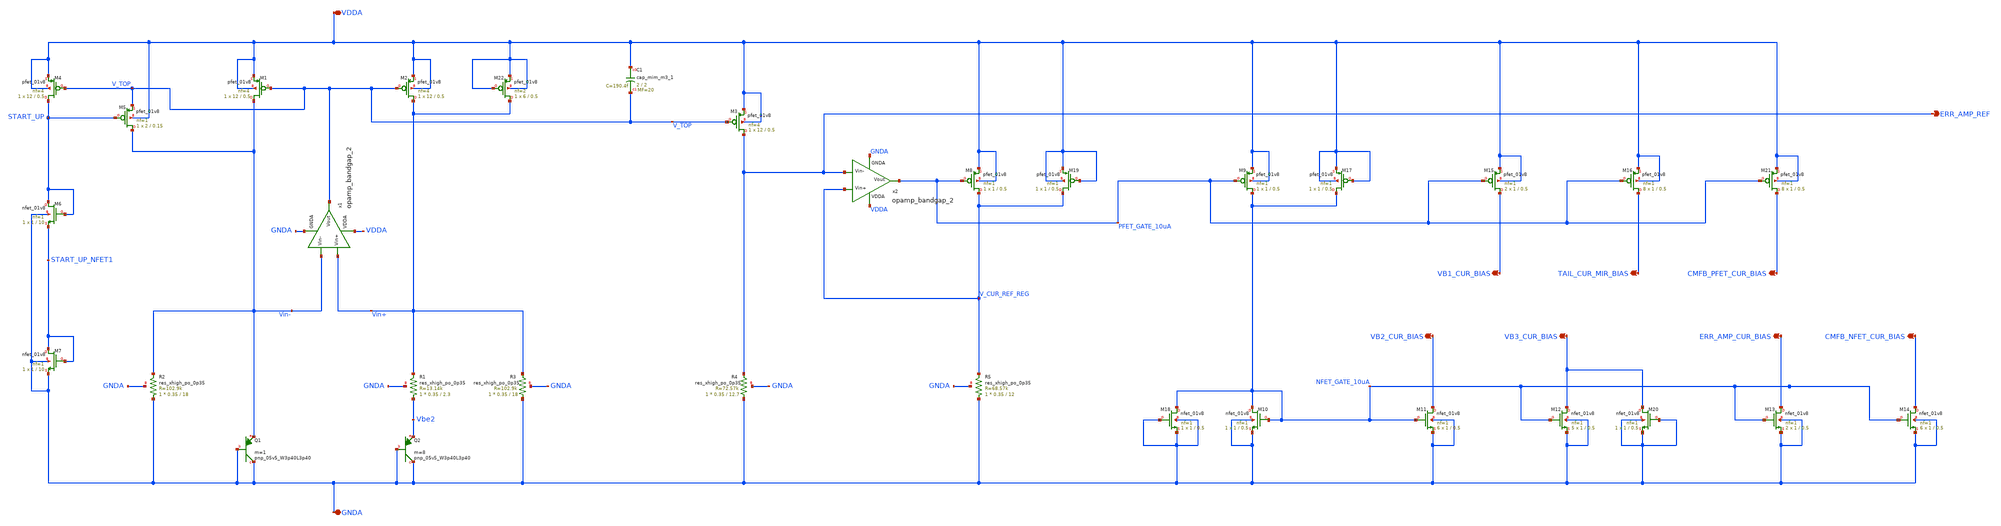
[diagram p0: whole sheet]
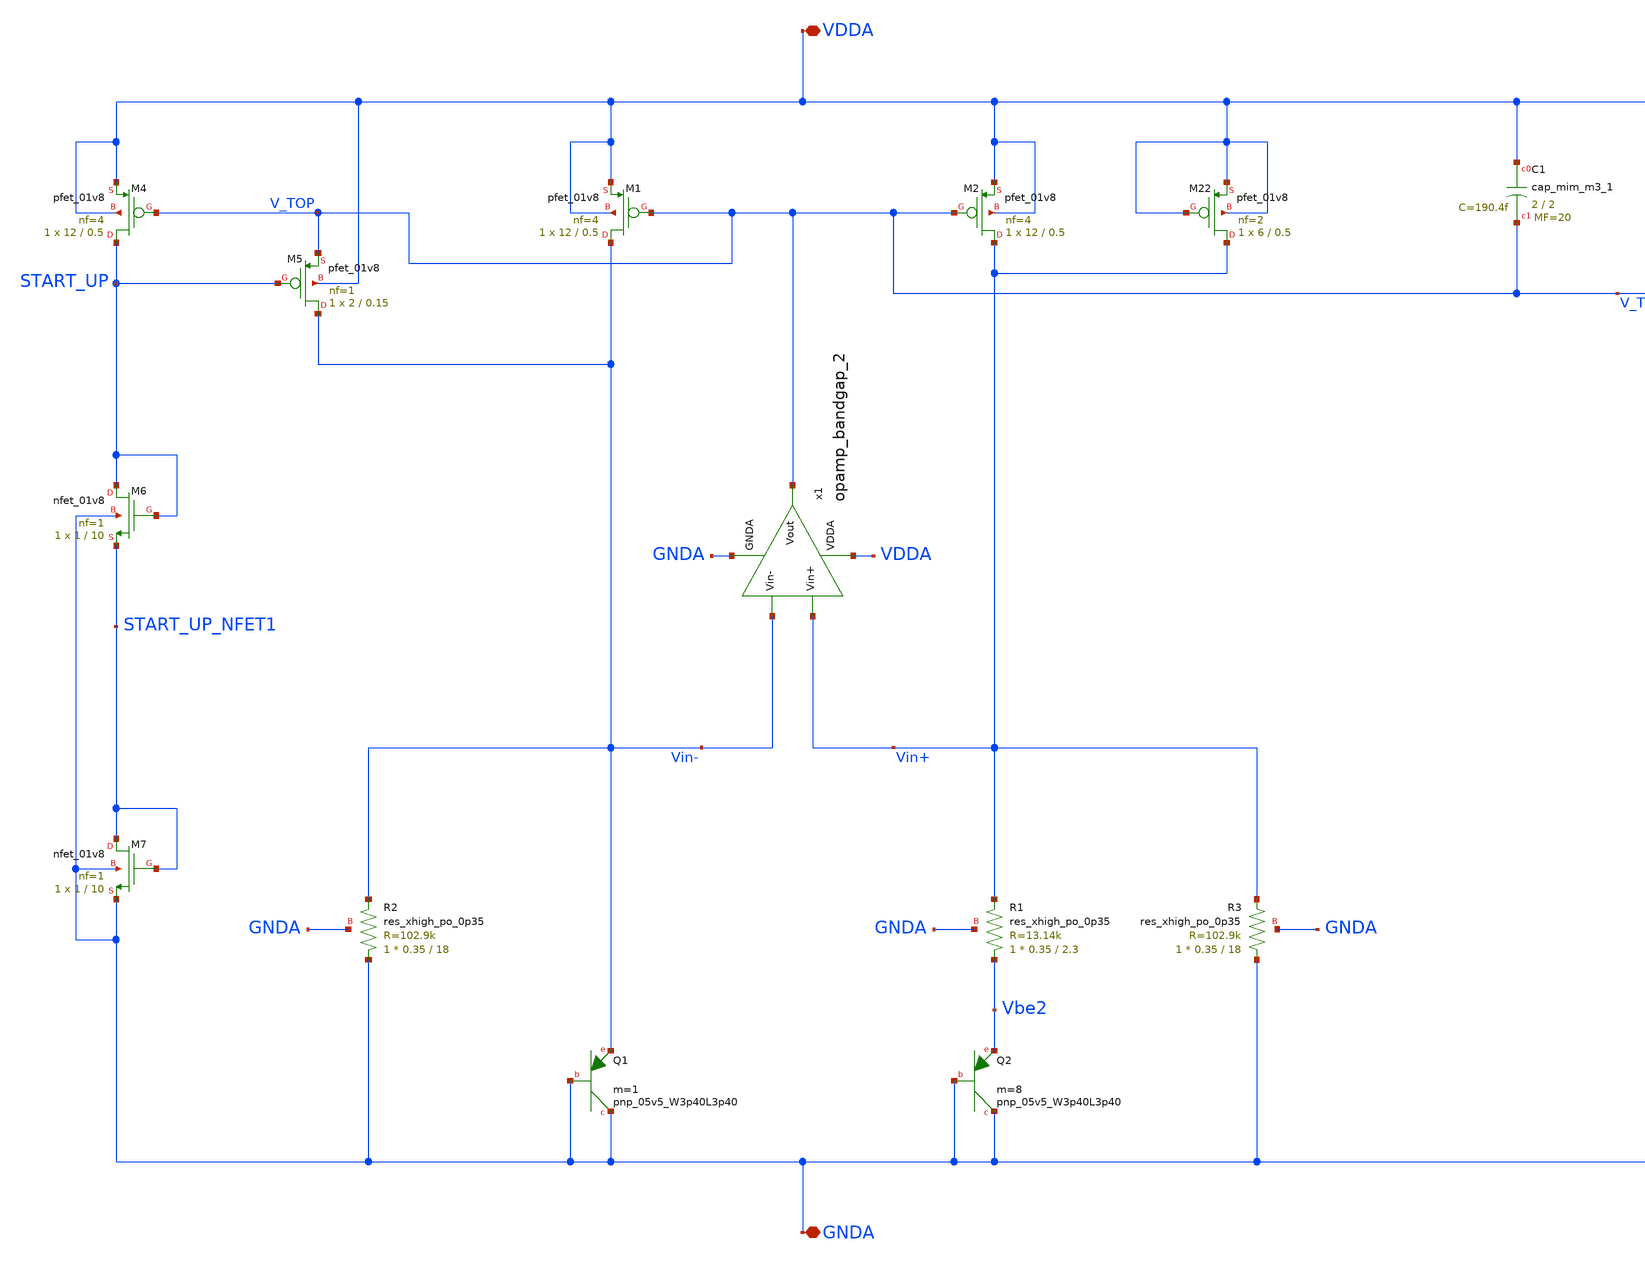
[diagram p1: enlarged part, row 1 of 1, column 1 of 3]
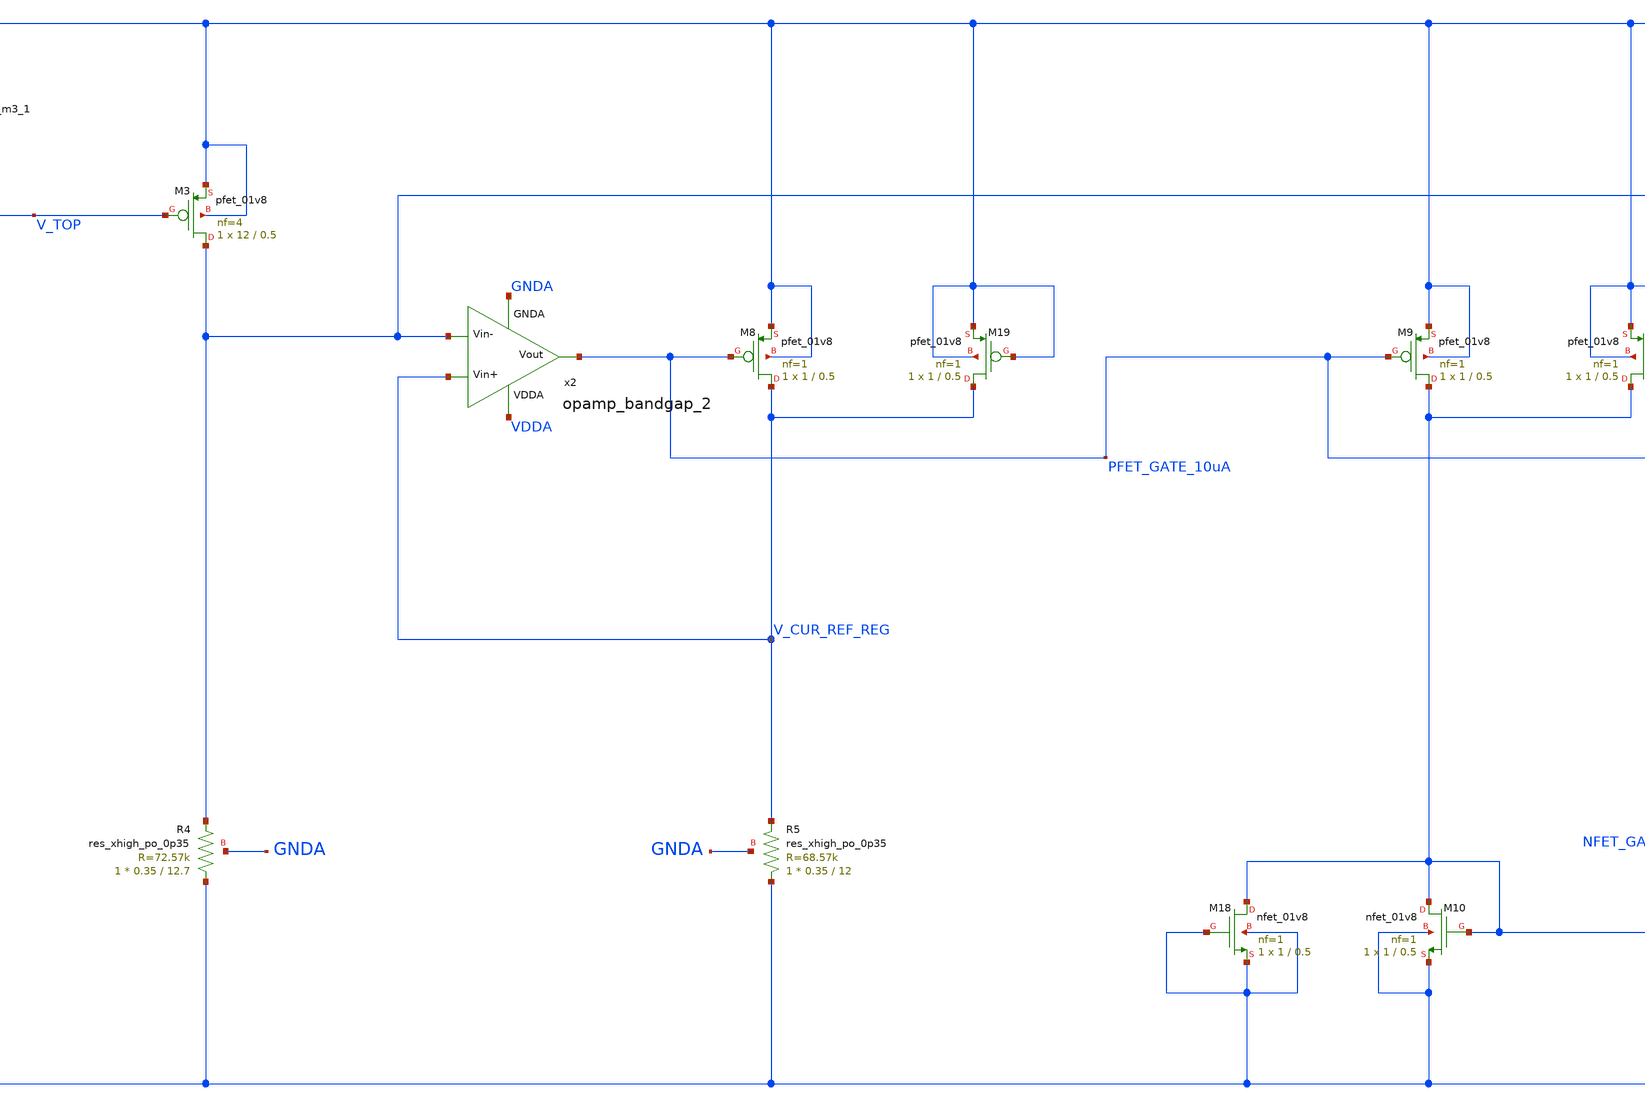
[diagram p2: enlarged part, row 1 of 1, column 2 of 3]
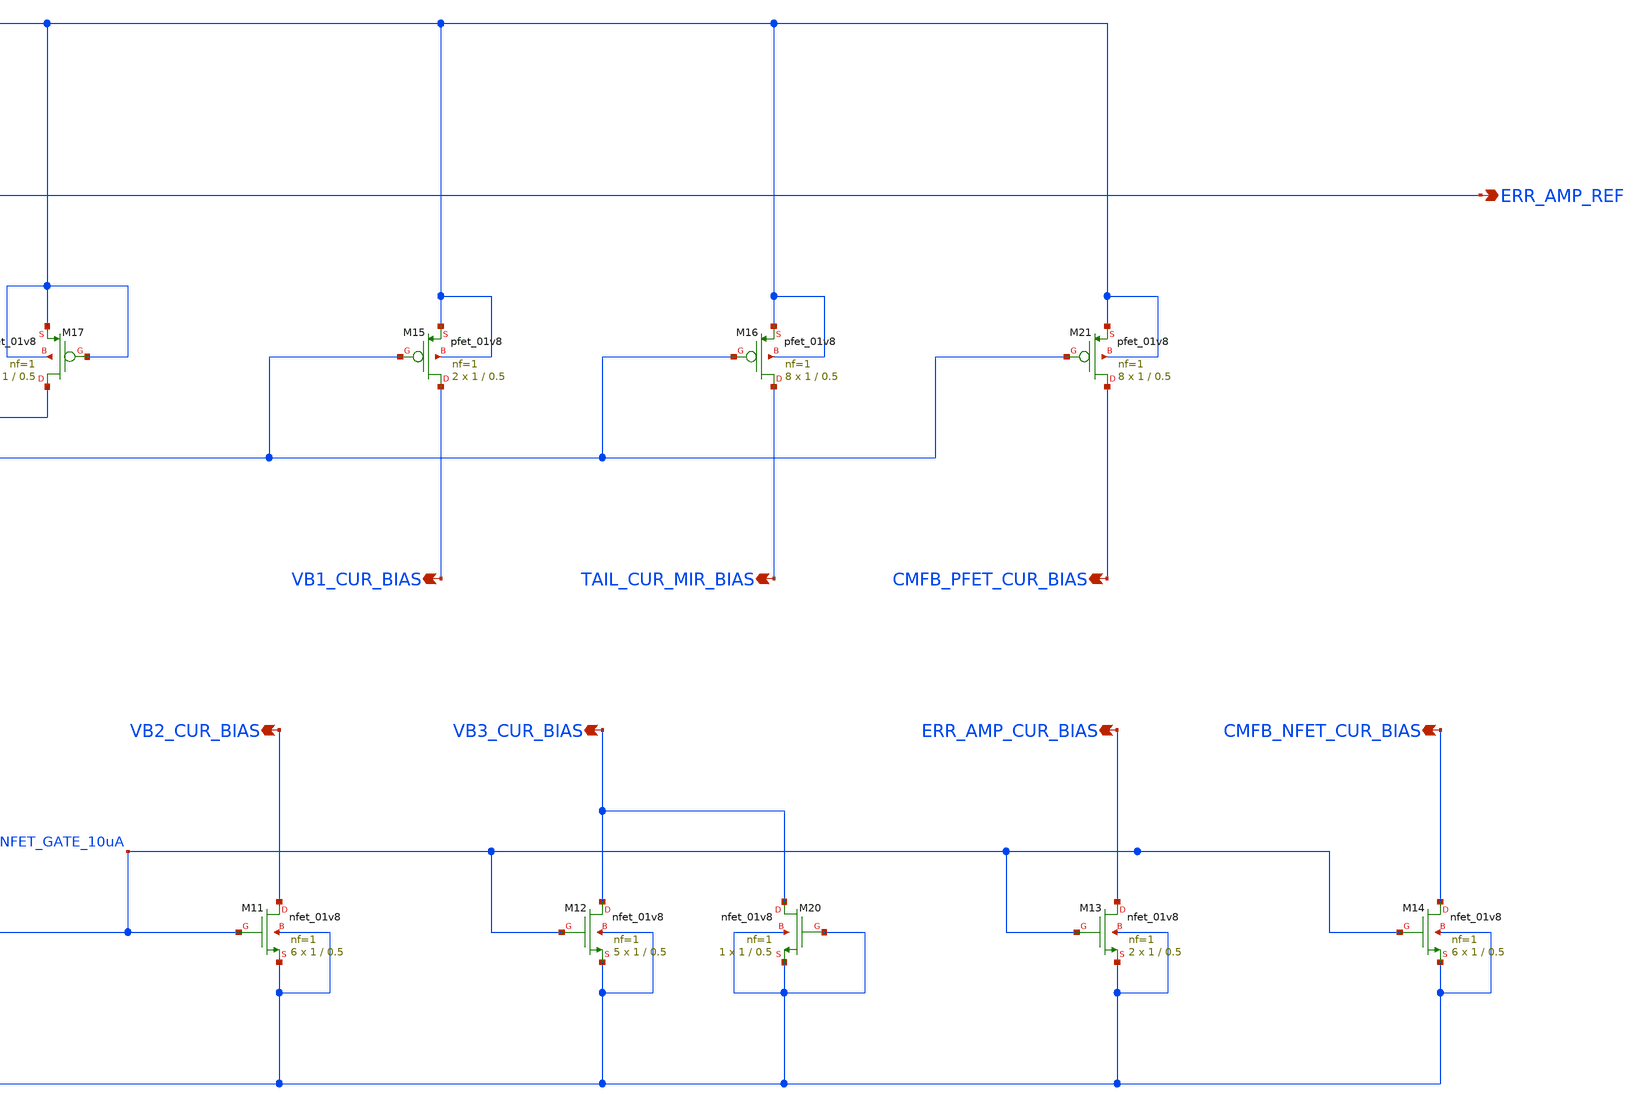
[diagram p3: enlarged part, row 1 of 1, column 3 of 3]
** sch_path: projects/opamp/xschem_ngspice/ref_volt_cur_gen_dummy.sch
**.subckt ref_volt_cur_gen_dummy VB1_CUR_BIAS GNDA ERR_AMP_REF VDDA VB2_CUR_BIAS VB3_CUR_BIAS
*+ ERR_AMP_CUR_BIAS CMFB_NFET_CUR_BIAS TAIL_CUR_MIR_BIAS CMFB_PFET_CUR_BIAS
*.opin VB1_CUR_BIAS
*.iopin GNDA
*.opin ERR_AMP_REF
*.iopin VDDA
*.opin VB2_CUR_BIAS
*.opin VB3_CUR_BIAS
*.opin ERR_AMP_CUR_BIAS
*.opin CMFB_NFET_CUR_BIAS
*.opin TAIL_CUR_MIR_BIAS
*.opin CMFB_PFET_CUR_BIAS
XM3 ERR_AMP_REF V_TOP VDDA VDDA sky130_fd_pr__pfet_01v8 L=0.5 W=12 nf=4 ad='int((nf+1)/2) * W/nf * 0.29'
+ as='int((nf+2)/2) * W/nf * 0.29' pd='2*int((nf+1)/2) * (W/nf + 0.29)' ps='2*int((nf+2)/2) * (W/nf + 0.29)'
+ nrd='0.29 / W' nrs='0.29 / W' sa=0 sb=0 sd=0 mult=1 m=1
XR4 GNDA ERR_AMP_REF GNDA sky130_fd_pr__res_xhigh_po_0p35 L=12.7 mult=1 m=1
XR5 GNDA V_CUR_REF_REG GNDA sky130_fd_pr__res_xhigh_po_0p35 L=12 mult=1 m=1
XM8 V_CUR_REF_REG PFET_GATE_10uA VDDA VDDA sky130_fd_pr__pfet_01v8 L=0.5 W=1 nf=1 ad='int((nf+1)/2) * W/nf * 0.29'
+ as='int((nf+2)/2) * W/nf * 0.29' pd='2*int((nf+1)/2) * (W/nf + 0.29)' ps='2*int((nf+2)/2) * (W/nf + 0.29)'
+ nrd='0.29 / W' nrs='0.29 / W' sa=0 sb=0 sd=0 mult=1 m=1
XC1 VDDA V_TOP sky130_fd_pr__cap_mim_m3_1 W=2 L=2 MF=20 m=20
XQ1 GNDA GNDA Vin- sky130_fd_pr__pnp_05v5_W3p40L3p40 m=1
XQ2 GNDA GNDA Vbe2 sky130_fd_pr__pnp_05v5_W3p40L3p40 m=8
XM1 Vin- V_TOP VDDA VDDA sky130_fd_pr__pfet_01v8 L=0.5 W=12 nf=4 ad='int((nf+1)/2) * W/nf * 0.29' as='int((nf+2)/2) * W/nf * 0.29'
+ pd='2*int((nf+1)/2) * (W/nf + 0.29)' ps='2*int((nf+2)/2) * (W/nf + 0.29)' nrd='0.29 / W' nrs='0.29 / W'
+ sa=0 sb=0 sd=0 mult=1 m=1
XM2 Vin+ V_TOP VDDA VDDA sky130_fd_pr__pfet_01v8 L=0.5 W=12 nf=4 ad='int((nf+1)/2) * W/nf * 0.29' as='int((nf+2)/2) * W/nf * 0.29'
+ pd='2*int((nf+1)/2) * (W/nf + 0.29)' ps='2*int((nf+2)/2) * (W/nf + 0.29)' nrd='0.29 / W' nrs='0.29 / W'
+ sa=0 sb=0 sd=0 mult=1 m=1
XR1 Vbe2 Vin+ GNDA sky130_fd_pr__res_xhigh_po_0p35 L=2.3 mult=1 m=1
XR3 GNDA Vin+ GNDA sky130_fd_pr__res_xhigh_po_0p35 L=18 mult=1 m=1
XR2 GNDA Vin- GNDA sky130_fd_pr__res_xhigh_po_0p35 L=18 mult=1 m=1
XM6 START_UP START_UP START_UP_NFET1 GNDA sky130_fd_pr__nfet_01v8 L=10 W=1 nf=1 ad='int((nf+1)/2) * W/nf * 0.29'
+ as='int((nf+2)/2) * W/nf * 0.29' pd='2*int((nf+1)/2) * (W/nf + 0.29)' ps='2*int((nf+2)/2) * (W/nf + 0.29)'
+ nrd='0.29 / W' nrs='0.29 / W' sa=0 sb=0 sd=0 mult=1 m=1
XM4 START_UP V_TOP VDDA VDDA sky130_fd_pr__pfet_01v8 L=0.5 W=12 nf=4 ad='int((nf+1)/2) * W/nf * 0.29'
+ as='int((nf+2)/2) * W/nf * 0.29' pd='2*int((nf+1)/2) * (W/nf + 0.29)' ps='2*int((nf+2)/2) * (W/nf + 0.29)'
+ nrd='0.29 / W' nrs='0.29 / W' sa=0 sb=0 sd=0 mult=1 m=1
XM5 Vin- START_UP V_TOP VDDA sky130_fd_pr__pfet_01v8 L=0.15 W=2 nf=1 ad='int((nf+1)/2) * W/nf * 0.29'
+ as='int((nf+2)/2) * W/nf * 0.29' pd='2*int((nf+1)/2) * (W/nf + 0.29)' ps='2*int((nf+2)/2) * (W/nf + 0.29)'
+ nrd='0.29 / W' nrs='0.29 / W' sa=0 sb=0 sd=0 mult=1 m=1
XM7 START_UP_NFET1 START_UP_NFET1 GNDA GNDA sky130_fd_pr__nfet_01v8 L=10 W=1 nf=1 ad='int((nf+1)/2) * W/nf * 0.29'
+ as='int((nf+2)/2) * W/nf * 0.29' pd='2*int((nf+1)/2) * (W/nf + 0.29)' ps='2*int((nf+2)/2) * (W/nf + 0.29)'
+ nrd='0.29 / W' nrs='0.29 / W' sa=0 sb=0 sd=0 mult=1 m=1
x1 VDDA V_TOP Vin- Vin+ GNDA opamp_bandgap_2
x2 VDDA PFET_GATE_10uA ERR_AMP_REF V_CUR_REF_REG GNDA opamp_bandgap_2
XM9 NFET_GATE_10uA PFET_GATE_10uA VDDA VDDA sky130_fd_pr__pfet_01v8 L=0.5 W=1 nf=1 ad='int((nf+1)/2) * W/nf * 0.29'
+ as='int((nf+2)/2) * W/nf * 0.29' pd='2*int((nf+1)/2) * (W/nf + 0.29)' ps='2*int((nf+2)/2) * (W/nf + 0.29)'
+ nrd='0.29 / W' nrs='0.29 / W' sa=0 sb=0 sd=0 mult=1 m=1
XM10 NFET_GATE_10uA NFET_GATE_10uA GNDA GNDA sky130_fd_pr__nfet_01v8 L=0.5 W=1 nf=1 ad='int((nf+1)/2) * W/nf * 0.29'
+ as='int((nf+2)/2) * W/nf * 0.29' pd='2*int((nf+1)/2) * (W/nf + 0.29)' ps='2*int((nf+2)/2) * (W/nf + 0.29)'
+ nrd='0.29 / W' nrs='0.29 / W' sa=0 sb=0 sd=0 mult=1 m=1
XM11 VB2_CUR_BIAS NFET_GATE_10uA GNDA GNDA sky130_fd_pr__nfet_01v8 L=0.5 W=1 nf=1 ad='int((nf+1)/2) * W/nf * 0.29'
+ as='int((nf+2)/2) * W/nf * 0.29' pd='2*int((nf+1)/2) * (W/nf + 0.29)' ps='2*int((nf+2)/2) * (W/nf + 0.29)'
+ nrd='0.29 / W' nrs='0.29 / W' sa=0 sb=0 sd=0 mult=6 m=6
XM12 VB3_CUR_BIAS NFET_GATE_10uA GNDA GNDA sky130_fd_pr__nfet_01v8 L=0.5 W=1 nf=1 ad='int((nf+1)/2) * W/nf * 0.29'
+ as='int((nf+2)/2) * W/nf * 0.29' pd='2*int((nf+1)/2) * (W/nf + 0.29)' ps='2*int((nf+2)/2) * (W/nf + 0.29)'
+ nrd='0.29 / W' nrs='0.29 / W' sa=0 sb=0 sd=0 mult=5 m=5
XM15 VB1_CUR_BIAS PFET_GATE_10uA VDDA VDDA sky130_fd_pr__pfet_01v8 L=0.5 W=1 nf=1 ad='int((nf+1)/2) * W/nf * 0.29'
+ as='int((nf+2)/2) * W/nf * 0.29' pd='2*int((nf+1)/2) * (W/nf + 0.29)' ps='2*int((nf+2)/2) * (W/nf + 0.29)'
+ nrd='0.29 / W' nrs='0.29 / W' sa=0 sb=0 sd=0 mult=2 m=2
XM13 ERR_AMP_CUR_BIAS NFET_GATE_10uA GNDA GNDA sky130_fd_pr__nfet_01v8 L=0.5 W=1 nf=1 ad='int((nf+1)/2) * W/nf * 0.29'
+ as='int((nf+2)/2) * W/nf * 0.29' pd='2*int((nf+1)/2) * (W/nf + 0.29)' ps='2*int((nf+2)/2) * (W/nf + 0.29)'
+ nrd='0.29 / W' nrs='0.29 / W' sa=0 sb=0 sd=0 mult=2 m=2
XM14 CMFB_NFET_CUR_BIAS NFET_GATE_10uA GNDA GNDA sky130_fd_pr__nfet_01v8 L=0.5 W=1 nf=1 ad='int((nf+1)/2) * W/nf * 0.29'
+ as='int((nf+2)/2) * W/nf * 0.29' pd='2*int((nf+1)/2) * (W/nf + 0.29)' ps='2*int((nf+2)/2) * (W/nf + 0.29)'
+ nrd='0.29 / W' nrs='0.29 / W' sa=0 sb=0 sd=0 mult=6 m=6
XM16 TAIL_CUR_MIR_BIAS PFET_GATE_10uA VDDA VDDA sky130_fd_pr__pfet_01v8 L=0.5 W=1 nf=1 ad='int((nf+1)/2) * W/nf * 0.29'
+ as='int((nf+2)/2) * W/nf * 0.29' pd='2*int((nf+1)/2) * (W/nf + 0.29)' ps='2*int((nf+2)/2) * (W/nf + 0.29)'
+ nrd='0.29 / W' nrs='0.29 / W' sa=0 sb=0 sd=0 mult=8 m=8
XM17 NFET_GATE_10uA VDDA VDDA VDDA sky130_fd_pr__pfet_01v8 L=0.5 W=1 nf=1 ad='int((nf+1)/2) * W/nf * 0.29'
+ as='int((nf+2)/2) * W/nf * 0.29' pd='2*int((nf+1)/2) * (W/nf + 0.29)' ps='2*int((nf+2)/2) * (W/nf + 0.29)'
+ nrd='0.29 / W' nrs='0.29 / W' sa=0 sb=0 sd=0 mult=1 m=1
XM18 NFET_GATE_10uA GNDA GNDA GNDA sky130_fd_pr__nfet_01v8 L=0.5 W=1 nf=1 ad='int((nf+1)/2) * W/nf * 0.29'
+ as='int((nf+2)/2) * W/nf * 0.29' pd='2*int((nf+1)/2) * (W/nf + 0.29)' ps='2*int((nf+2)/2) * (W/nf + 0.29)'
+ nrd='0.29 / W' nrs='0.29 / W' sa=0 sb=0 sd=0 mult=1 m=1
XM19 V_CUR_REF_REG VDDA VDDA VDDA sky130_fd_pr__pfet_01v8 L=0.5 W=1 nf=1 ad='int((nf+1)/2) * W/nf * 0.29'
+ as='int((nf+2)/2) * W/nf * 0.29' pd='2*int((nf+1)/2) * (W/nf + 0.29)' ps='2*int((nf+2)/2) * (W/nf + 0.29)'
+ nrd='0.29 / W' nrs='0.29 / W' sa=0 sb=0 sd=0 mult=1 m=1
XM20 VB3_CUR_BIAS GNDA GNDA GNDA sky130_fd_pr__nfet_01v8 L=0.5 W=1 nf=1 ad='int((nf+1)/2) * W/nf * 0.29'
+ as='int((nf+2)/2) * W/nf * 0.29' pd='2*int((nf+1)/2) * (W/nf + 0.29)' ps='2*int((nf+2)/2) * (W/nf + 0.29)'
+ nrd='0.29 / W' nrs='0.29 / W' sa=0 sb=0 sd=0 mult=1 m=1
XM21 CMFB_PFET_CUR_BIAS PFET_GATE_10uA VDDA VDDA sky130_fd_pr__pfet_01v8 L=0.5 W=1 nf=1 ad='int((nf+1)/2) * W/nf * 0.29'
+ as='int((nf+2)/2) * W/nf * 0.29' pd='2*int((nf+1)/2) * (W/nf + 0.29)' ps='2*int((nf+2)/2) * (W/nf + 0.29)'
+ nrd='0.29 / W' nrs='0.29 / W' sa=0 sb=0 sd=0 mult=8 m=8
XM22 Vin+ VDDA VDDA VDDA sky130_fd_pr__pfet_01v8 L=0.5 W=6 nf=2 ad='int((nf+1)/2) * W/nf * 0.29' as='int((nf+2)/2) * W/nf * 0.29'
+ pd='2*int((nf+1)/2) * (W/nf + 0.29)' ps='2*int((nf+2)/2) * (W/nf + 0.29)' nrd='0.29 / W' nrs='0.29 / W'
+ sa=0 sb=0 sd=0 mult=1 m=1
**.ends

* expanding   symbol:
*+  /foss/designs/my_design/projects/bandgapref/xschem_ngspice/new_files/opamp_bandgap_2.sym # of pins=5
** sym_path: projects/bandgapref/xschem_ngspice/new_files/opamp_bandgap_2.sym
** sch_path: projects/bandgapref/xschem_ngspice/new_files/opamp_bandgap_2.sch
.subckt opamp_bandgap_2 VDDA Vout Vin- Vin+ GNDA
*.ipin Vin+
*.opin Vout
*.ipin Vin-
*.ipin GNDA
*.ipin VDDA
XM1 V_p VDDA GNDA GNDA sky130_fd_pr__nfet_01v8 L=5 W=2.5 nf=1 ad='int((nf+1)/2) * W/nf * 0.29' as='int((nf+2)/2) * W/nf * 0.29'
+ pd='2*int((nf+1)/2) * (W/nf + 0.29)' ps='2*int((nf+2)/2) * (W/nf + 0.29)' nrd='0.29 / W' nrs='0.29 / W'
+ sa=0 sb=0 sd=0 mult=1 m=1
XM2 V_mirror Vin- V_p GNDA sky130_fd_pr__nfet_01v8 L=0.2 W=2.5 nf=1 ad='int((nf+1)/2) * W/nf * 0.29'
+ as='int((nf+2)/2) * W/nf * 0.29' pd='2*int((nf+1)/2) * (W/nf + 0.29)' ps='2*int((nf+2)/2) * (W/nf + 0.29)'
+ nrd='0.29 / W' nrs='0.29 / W' sa=0 sb=0 sd=0 mult=1 m=1
XM3 1st_Vout Vin+ V_p GNDA sky130_fd_pr__nfet_01v8 L=0.2 W=2.5 nf=1 ad='int((nf+1)/2) * W/nf * 0.29'
+ as='int((nf+2)/2) * W/nf * 0.29' pd='2*int((nf+1)/2) * (W/nf + 0.29)' ps='2*int((nf+2)/2) * (W/nf + 0.29)'
+ nrd='0.29 / W' nrs='0.29 / W' sa=0 sb=0 sd=0 mult=1 m=1
XM5 V_mirror V_mirror VDDA VDDA sky130_fd_pr__pfet_01v8 L=0.2 W=6 nf=2 ad='int((nf+1)/2) * W/nf * 0.29'
+ as='int((nf+2)/2) * W/nf * 0.29' pd='2*int((nf+1)/2) * (W/nf + 0.29)' ps='2*int((nf+2)/2) * (W/nf + 0.29)'
+ nrd='0.29 / W' nrs='0.29 / W' sa=0 sb=0 sd=0 mult=1 m=1
XM6 1st_Vout V_mirror VDDA VDDA sky130_fd_pr__pfet_01v8 L=0.2 W=6 nf=2 ad='int((nf+1)/2) * W/nf * 0.29'
+ as='int((nf+2)/2) * W/nf * 0.29' pd='2*int((nf+1)/2) * (W/nf + 0.29)' ps='2*int((nf+2)/2) * (W/nf + 0.29)'
+ nrd='0.29 / W' nrs='0.29 / W' sa=0 sb=0 sd=0 mult=1 m=1
XM4 Vout VDDA GNDA GNDA sky130_fd_pr__nfet_01v8 L=5 W=2.5 nf=1 ad='int((nf+1)/2) * W/nf * 0.29' as='int((nf+2)/2) * W/nf * 0.29'
+ pd='2*int((nf+1)/2) * (W/nf + 0.29)' ps='2*int((nf+2)/2) * (W/nf + 0.29)' nrd='0.29 / W' nrs='0.29 / W'
+ sa=0 sb=0 sd=0 mult=1 m=1
XM7 Vout 1st_Vout VDDA VDDA sky130_fd_pr__pfet_01v8 L=0.2 W=6 nf=2 ad='int((nf+1)/2) * W/nf * 0.29' as='int((nf+2)/2) * W/nf * 0.29'
+ pd='2*int((nf+1)/2) * (W/nf + 0.29)' ps='2*int((nf+2)/2) * (W/nf + 0.29)' nrd='0.29 / W' nrs='0.29 / W'
+ sa=0 sb=0 sd=0 mult=1 m=1
XC1 1st_Vout cap_res sky130_fd_pr__cap_mim_m3_1 W=2 L=2 MF=20 m=20
XM8 Vout VDDA VDDA VDDA sky130_fd_pr__pfet_01v8 L=0.2 W=2 nf=2 ad='int((nf+1)/2) * W/nf * 0.29' as='int((nf+2)/2) * W/nf * 0.29'
+ pd='2*int((nf+1)/2) * (W/nf + 0.29)' ps='2*int((nf+2)/2) * (W/nf + 0.29)' nrd='0.29 / W' nrs='0.29 / W'
+ sa=0 sb=0 sd=0 mult=1 m=1
XR2 Vout cap_res GNDA sky130_fd_pr__res_high_po_0p35 L=2.05 mult=1 m=1
.ends

.end
